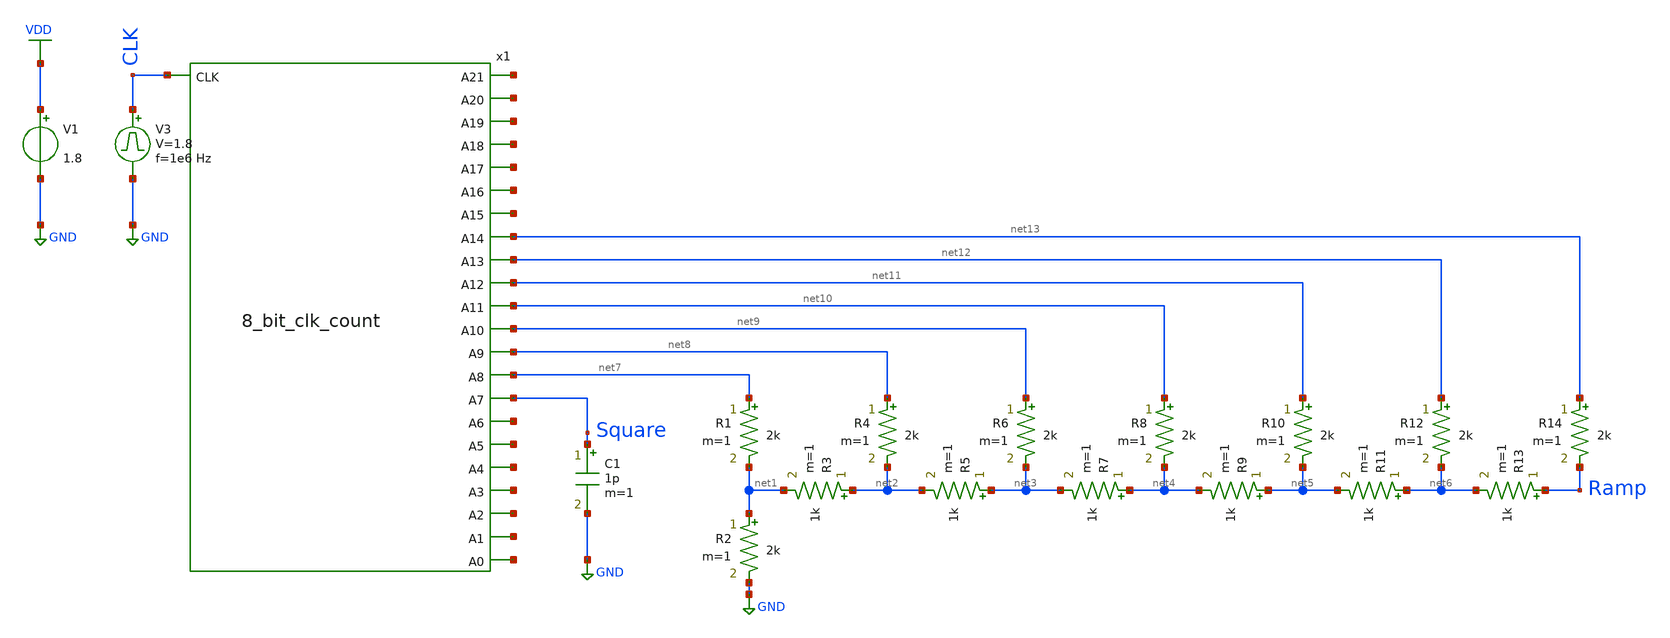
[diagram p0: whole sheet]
** sch_path: library/xschem/8_bit_count_tb.sch
**.subckt 8_bit_count_tb
V1 VDD GND 1.8
C1 Square GND 1p m=1
V3 CLK GND pulse 0 1.8 '0.495/ 1e6 ' '0.01/1e6 ' '0.01/1e6 ' '0.49/1e6 ' '1/1e6 '
x1 net14 net15 net16 net17 net18 net19 net20 net21 net22 net23 Square net24 net25 net26 net27 CLK
+ net12 net11 net10 net9 net13 net8 net7 8_bit_clk_count
R1 net7 net1 2k m=1
R2 net1 GND 2k m=1
R3 net2 net1 1k m=1
R4 net8 net2 2k m=1
R5 net3 net2 1k m=1
R6 net9 net3 2k m=1
R7 net4 net3 1k m=1
R8 net10 net4 2k m=1
R9 net5 net4 1k m=1
R10 net11 net5 2k m=1
R11 net6 net5 1k m=1
R12 net12 net6 2k m=1
R13 Ramp net6 1k m=1
R14 net13 Ramp 2k m=1
**** begin user architecture code


.control
save all
tran 1n 100u
plot V(CLK) V(Square)+2 V(Ramp)+4
.endc


** opencircuitdesign pdks install
.lib $::SKYWATER_MODELS/sky130.lib.spice tt


**** end user architecture code
**.ends
.GLOBAL VDD
.GLOBAL GND
.end
